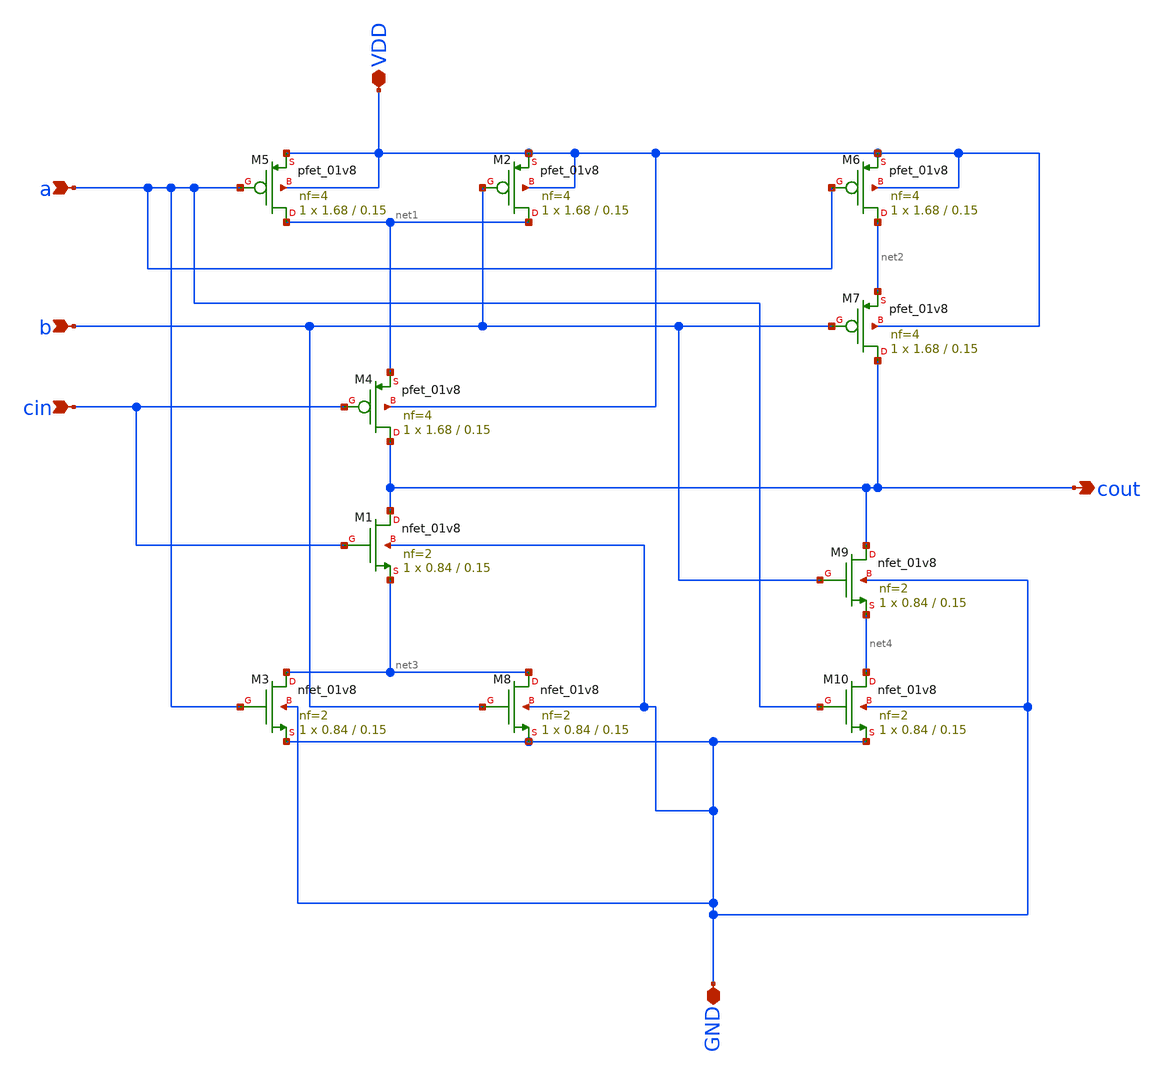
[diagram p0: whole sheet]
** sch_path: assignments/assignment8/carry.sch
**.subckt carry cout a VDD GND b cin
*.opin cout
*.ipin a
*.iopin VDD
*.iopin GND
*.ipin b
*.ipin cin
XM1 cout cin net3 GND sky130_fd_pr__nfet_01v8 L=0.15 W=0.84 nf=2 ad='int((nf+1)/2) * W/nf * 0.29' as='int((nf+2)/2) * W/nf * 0.29'
+ pd='2*int((nf+1)/2) * (W/nf + 0.29)' ps='2*int((nf+2)/2) * (W/nf + 0.29)' nrd='0.29 / W' nrs='0.29 / W'
+ sa=0 sb=0 sd=0 mult=1 m=1
XM2 net1 b VDD VDD sky130_fd_pr__pfet_01v8 L=0.15 W=1.68 nf=4 ad='int((nf+1)/2) * W/nf * 0.29' as='int((nf+2)/2) * W/nf * 0.29'
+ pd='2*int((nf+1)/2) * (W/nf + 0.29)' ps='2*int((nf+2)/2) * (W/nf + 0.29)' nrd='0.29 / W' nrs='0.29 / W'
+ sa=0 sb=0 sd=0 mult=1 m=1
XM3 net3 a GND GND sky130_fd_pr__nfet_01v8 L=0.15 W=0.84 nf=2 ad='int((nf+1)/2) * W/nf * 0.29' as='int((nf+2)/2) * W/nf * 0.29'
+ pd='2*int((nf+1)/2) * (W/nf + 0.29)' ps='2*int((nf+2)/2) * (W/nf + 0.29)' nrd='0.29 / W' nrs='0.29 / W'
+ sa=0 sb=0 sd=0 mult=1 m=1
XM4 cout cin net1 VDD sky130_fd_pr__pfet_01v8 L=0.15 W=1.68 nf=4 ad='int((nf+1)/2) * W/nf * 0.29' as='int((nf+2)/2) * W/nf * 0.29'
+ pd='2*int((nf+1)/2) * (W/nf + 0.29)' ps='2*int((nf+2)/2) * (W/nf + 0.29)' nrd='0.29 / W' nrs='0.29 / W'
+ sa=0 sb=0 sd=0 mult=1 m=1
XM5 net1 a VDD VDD sky130_fd_pr__pfet_01v8 L=0.15 W=1.68 nf=4 ad='int((nf+1)/2) * W/nf * 0.29' as='int((nf+2)/2) * W/nf * 0.29'
+ pd='2*int((nf+1)/2) * (W/nf + 0.29)' ps='2*int((nf+2)/2) * (W/nf + 0.29)' nrd='0.29 / W' nrs='0.29 / W'
+ sa=0 sb=0 sd=0 mult=1 m=1
XM6 net2 a VDD VDD sky130_fd_pr__pfet_01v8 L=0.15 W=1.68 nf=4 ad='int((nf+1)/2) * W/nf * 0.29' as='int((nf+2)/2) * W/nf * 0.29'
+ pd='2*int((nf+1)/2) * (W/nf + 0.29)' ps='2*int((nf+2)/2) * (W/nf + 0.29)' nrd='0.29 / W' nrs='0.29 / W'
+ sa=0 sb=0 sd=0 mult=1 m=1
XM7 cout b net2 VDD sky130_fd_pr__pfet_01v8 L=0.15 W=1.68 nf=4 ad='int((nf+1)/2) * W/nf * 0.29' as='int((nf+2)/2) * W/nf * 0.29'
+ pd='2*int((nf+1)/2) * (W/nf + 0.29)' ps='2*int((nf+2)/2) * (W/nf + 0.29)' nrd='0.29 / W' nrs='0.29 / W'
+ sa=0 sb=0 sd=0 mult=1 m=1
XM8 net3 b GND GND sky130_fd_pr__nfet_01v8 L=0.15 W=0.84 nf=2 ad='int((nf+1)/2) * W/nf * 0.29' as='int((nf+2)/2) * W/nf * 0.29'
+ pd='2*int((nf+1)/2) * (W/nf + 0.29)' ps='2*int((nf+2)/2) * (W/nf + 0.29)' nrd='0.29 / W' nrs='0.29 / W'
+ sa=0 sb=0 sd=0 mult=1 m=1
XM9 cout b net4 GND sky130_fd_pr__nfet_01v8 L=0.15 W=0.84 nf=2 ad='int((nf+1)/2) * W/nf * 0.29' as='int((nf+2)/2) * W/nf * 0.29'
+ pd='2*int((nf+1)/2) * (W/nf + 0.29)' ps='2*int((nf+2)/2) * (W/nf + 0.29)' nrd='0.29 / W' nrs='0.29 / W'
+ sa=0 sb=0 sd=0 mult=1 m=1
XM10 net4 a GND GND sky130_fd_pr__nfet_01v8 L=0.15 W=0.84 nf=2 ad='int((nf+1)/2) * W/nf * 0.29' as='int((nf+2)/2) * W/nf * 0.29'
+ pd='2*int((nf+1)/2) * (W/nf + 0.29)' ps='2*int((nf+2)/2) * (W/nf + 0.29)' nrd='0.29 / W' nrs='0.29 / W'
+ sa=0 sb=0 sd=0 mult=1 m=1
**.ends
.end
